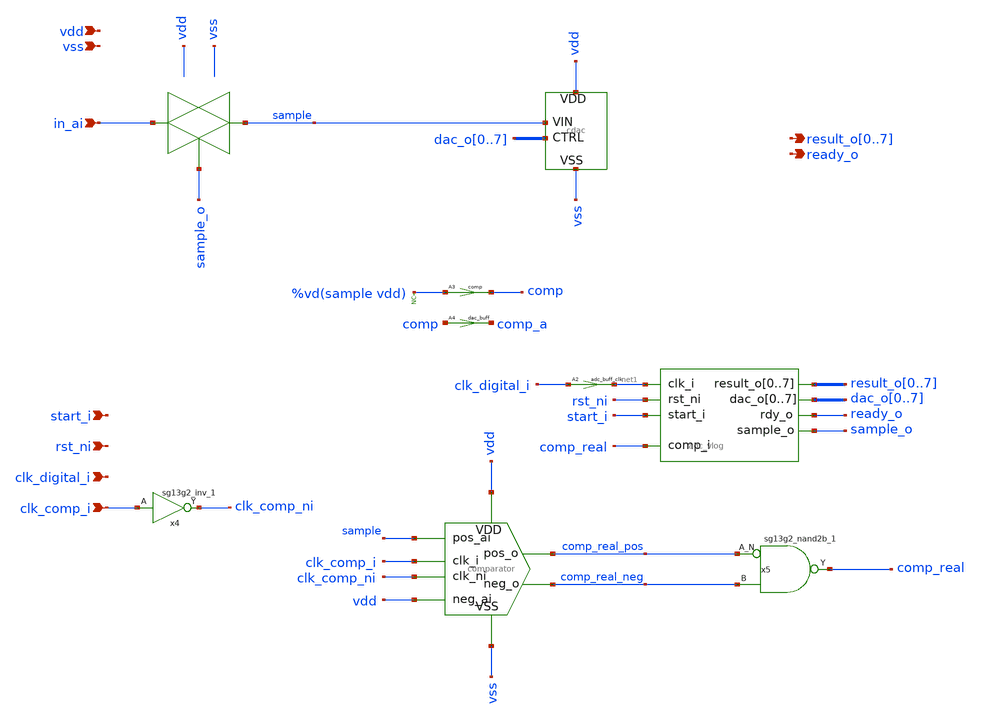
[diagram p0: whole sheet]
** sch_path: designs/basic1/adc.sch
* IHP-GmbH/IHP-Open-PDK/ihp-sg13g2/libs.tech/xschem/sg13g2_stdcells/sg13g2_inv_2.sch:
* Copyright 2023 IHP PDK Authors
* Licensed under the Apache License, Version 2.0 (the "License");
**.subckt adc in_ai clk_digital_i vss vdd rst_ni start_i ready_o
*+ result_o0,result_o1,result_o2,result_o3,result_o4,result_o5,result_o6,result_o7 clk_comp_i
*.ipin in_ai
*.ipin clk_digital_i
*.ipin vss
*.ipin vdd
*.ipin rst_ni
*.ipin start_i
*.opin ready_o
*.opin result_o0,result_o1,result_o2,result_o3,result_o4,result_o5,result_o6,result_o7
*.ipin clk_comp_i
x3 sample dac_o0 dac_o1 dac_o2 dac_o3 dac_o4 dac_o5 dac_o6 dac_o7 vss vdd cdac
A2 [ clk_digital_i ] [ net1 ] adc_buff_clk
A1 [ net1 start_i rst_ni comp_real ] [ ready_o sample_o dac_o0 dac_o1 dac_o2 dac_o3 dac_o4 dac_o5
+ dac_o6 dac_o7 result_o0 result_o1 result_o2 result_o3 result_o4 result_o5 result_o6 result_o7 ] adc
A3 [ %vd(sample vdd) ] [ comp ] comp
A4 [ comp ] [ comp_a ] dac_buff
* noconn %vd(sample vdd)
x2 clk_comp_i sample vdd comp_real_neg comp_real_pos vss vdd clk_comp_ni comparator
x4 clk_comp_ni clk_comp_i VDD VSS sg13g2_inv_1
x5 comp_real comp_real_pos comp_real_neg VDD VSS sg13g2_nand2b_1
**.ends

* expanding   symbol:  /workspaces/ngspice_cosim_inv/designs/cdac/cdac.sym # of pins=4
** sym_path: designs/cdac/cdac.sym
** sch_path: designs/cdac/cdac.sch
.subckt cdac VIN CTRL0 CTRL1 CTRL2 CTRL3 CTRL4 CTRL5 CTRL6 CTRL7 VSS VDD
*.ipin VIN
*.ipin CTRL0,CTRL1,CTRL2,CTRL3,CTRL4,CTRL5,CTRL6,CTRL7
*.ipin VSS
*.ipin VDD
XC2 VIN l1 cap_cmim w=7.297e-5 l=7.298e-5 m=1 mm_ok=1
XC3 VIN l2 cap_cmim w=5.158e-5 l=5.159e-5 m=1 mm_ok=1
XC4 VIN l3 cap_cmim w=3.646e-5 l=3.646e-5 m=1 mm_ok=1
XC5 VIN VSS cap_cmim w=6.402e-6 l=6.402e-6 m=1 mm_ok=1
x1 l1 CTRL0 VDD VSS sg13g2_inv_2
x2 l2 CTRL1 VDD VSS sg13g2_inv_2
x3 l3 CTRL2 VDD VSS sg13g2_inv_2
x4 l4 CTRL3 VDD VSS sg13g2_inv_2
XC6 VIN l4 cap_cmim w=2.577e-5 l=2.577e-5 m=1 mm_ok=1
XC7 VIN l5 cap_cmim w=1.820e-5 l=1.820e-5 m=1 mm_ok=1
XC8 VIN l6 cap_cmim w=1.286e-5 l=1.286e-5 m=1 mm_ok=1
XC9 VIN l7 cap_cmim w=9.077e-6 l=9.077e-6 m=1 mm_ok=1
x5 l5 CTRL4 VDD VSS sg13g2_inv_2
x6 l6 CTRL5 VDD VSS sg13g2_inv_2
x7 l7 CTRL6 VDD VSS sg13g2_inv_2
x8 l8 CTRL7 VDD VSS sg13g2_inv_2
XC1 VIN l8 cap_cmim w=6.402e-6 l=6.402e-6 m=1 mm_ok=1
.ends


* expanding   symbol:  /workspaces/ngspice_cosim_inv/designs/comparator_dt/comparator.sym # of
*+ pins=8
** sym_path: designs/comparator_dt/comparator.sym
** sch_path: designs/comparator_dt/comparator.sch
.subckt comparator clk_i pos_ai neg_ai neg_o pos_o VSS VDD clk_ni
*.ipin pos_ai
*.ipin neg_ai
*.ipin VSS
*.ipin VDD
*.opin neg_o
*.opin pos_o
*.ipin clk_i
*.ipin clk_ni
XM12 neg_buf clk_i VDD VDD sg13_lv_pmos w=1.0u l=0.13u ng=1 m=1 mm_ok=1
XM13 pos_buf clk_i VDD VDD sg13_lv_pmos w=1.0u l=0.13u ng=1 m=1 mm_ok=1
XM14 net1 pos_ai neg_buf VSS sg13_lv_nmos w=1.0u l=0.13u ng=1 m=1 mm_ok=1
XM15 net1 neg_ai pos_buf VSS sg13_lv_nmos w=1.0u l=0.13u ng=1 m=1 mm_ok=1
XM16 VSS clk_i net1 VSS sg13_lv_nmos w=1.0u l=0.13u ng=1 m=1 mm_ok=1
XM17 net2 clk_ni VDD VDD sg13_lv_pmos w=2.0u l=0.13u ng=2 m=1 mm_ok=1
XM18 pos_o neg_o net2 VDD sg13_lv_pmos w=2.0u l=0.13u ng=2 m=1 mm_ok=1
XM19 neg_o pos_o net2 VDD sg13_lv_pmos w=2.0u l=0.13u ng=2 m=1 mm_ok=1
XM20 VSS neg_buf pos_o VSS sg13_lv_nmos w=1.0u l=0.13u ng=1 m=1 mm_ok=1
XM21 VSS neg_o pos_o VSS sg13_lv_nmos w=1.0u l=0.13u ng=1 m=1 mm_ok=1
XM22 VSS pos_o neg_o VSS sg13_lv_nmos w=1.0u l=0.13u ng=1 m=1 mm_ok=1
XM23 VSS pos_buf neg_o VSS sg13_lv_nmos w=1.0u l=0.13u ng=1 m=1 mm_ok=1
XC1 neg_buf VSS cap_cmim w=1.41e-5 l=1.41e-5 m=1 mm_ok=1
XC2 pos_buf VSS cap_cmim w=1.41e-5 l=1.41e-5 m=1 mm_ok=1
.ends


* expanding   symbol:  sg13g2_stdcells/sg13g2_inv_1.sym # of pins=2
** sym_path: sg13g2_stdcells/sg13g2_inv_1.sym
** sch_path: sg13g2_stdcells/sg13g2_inv_1.sch
.subckt sg13g2_inv_1 Y A VDD VSS
*.opin Y
*.ipin A
*.iopin VDD
*.iopin VSS
XM1 Y A VSS VSS sg13_lv_nmos w=740.00n l=130.00n ng=1 m=1 mm_ok=1
XM2 Y A VDD VDD sg13_lv_pmos w=1.12u l=130.00n ng=1 m=1 mm_ok=1
.ends


* expanding   symbol:  sg13g2_stdcells/sg13g2_nand2b_1.sym # of pins=3
** sym_path: sg13g2_stdcells/sg13g2_nand2b_1.sym
** sch_path: sg13g2_stdcells/sg13g2_nand2b_1.sch
.subckt sg13g2_nand2b_1 Y A_N B VDD VSS
*.opin Y
*.ipin B
*.ipin A_N
*.iopin VDD
*.iopin VSS
XM1 net1 A_N VSS VSS sg13_lv_nmos w=550.00n l=130.00n ng=1 m=1 mm_ok=1
XM2 Y net1 net2 VSS sg13_lv_nmos w=740.00n l=130.00n ng=1 m=1 mm_ok=1
XM3 net2 B VSS VSS sg13_lv_nmos w=740.00n l=130.00n ng=1 m=1 mm_ok=1
XM4 Y B VDD VDD sg13_lv_pmos w=1.12u l=130.00n ng=1 m=1 mm_ok=1
XM5 net1 A_N VDD VDD sg13_lv_pmos w=840.00n l=130.00n ng=1 m=1 mm_ok=1
XM6 Y net1 VDD VDD sg13_lv_pmos w=1.12u l=130.00n ng=1 m=1 mm_ok=1
.ends


* expanding   symbol:  sg13g2_stdcells/sg13g2_inv_2.sym # of pins=2
** sym_path: sg13g2_stdcells/sg13g2_inv_2.sym
** sch_path: sg13g2_stdcells/sg13g2_inv_2.sch
.subckt sg13g2_inv_2 Y A VDD VSS
*.opin Y
*.ipin A
*.iopin VDD
*.iopin VSS
XM1 Y A VSS VSS sg13_lv_nmos w=1.48u l=130.00n ng=2 m=1 mm_ok=1
XM2 Y A VDD VDD sg13_lv_pmos w=2.24u l=130.00n ng=2 m=1 mm_ok=1
.ends

**** begin user architecture code
.model adc d_cosim simulation="ivlng" sim_args=["adc"]
.model dac_buff dac_bridge input_load=1e-15 t_rise=0.1n t_fall=0.1n  out_low=0 out_high=1.5
.model comp adc_bridge in_low=0 in_high=0
**** end user architecture code
.end
